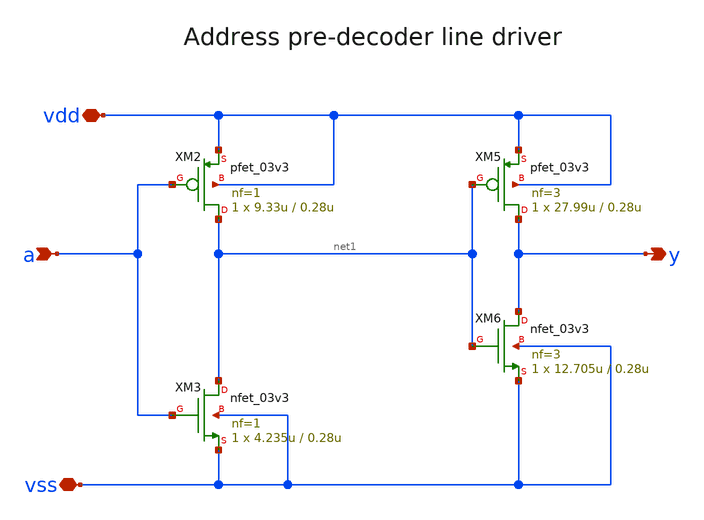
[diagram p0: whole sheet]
** sch_path: cells/gf180mcu_ocd_ip_sram__sram512x8m8wm1/xschem/ypredec1_ys_3v512x8m81.sch
**.subckt ypredec1_ys_3v512x8m81 vdd vss a y
*.iopin vdd
*.iopin vss
*.ipin a
*.opin y
XM2 net1 a vdd vdd pfet_03v3 L=0.28u W=9.33u nf=1 ad='int((nf+1)/2) * W/nf * 0.18u' as='int((nf+2)/2) * W/nf * 0.18u'
+ pd='2*int((nf+1)/2) * (W/nf + 0.18u)' ps='2*int((nf+2)/2) * (W/nf + 0.18u)' nrd='0.18u / W' nrs='0.18u / W'
+ sa=0 sb=0 sd=0 m=1
XM3 net1 a vss vss nfet_03v3 L=0.28u W=4.235u nf=1 ad='int((nf+1)/2) * W/nf * 0.18u' as='int((nf+2)/2) * W/nf * 0.18u'
+ pd='2*int((nf+1)/2) * (W/nf + 0.18u)' ps='2*int((nf+2)/2) * (W/nf + 0.18u)' nrd='0.18u / W' nrs='0.18u / W'
+ sa=0 sb=0 sd=0 m=1
XM5 y net1 vdd vdd pfet_03v3 L=0.28u W=27.99u nf=3 ad='int((nf+1)/2) * W/nf * 0.18u' as='int((nf+2)/2) * W/nf * 0.18u'
+ pd='2*int((nf+1)/2) * (W/nf + 0.18u)' ps='2*int((nf+2)/2) * (W/nf + 0.18u)' nrd='0.18u / W' nrs='0.18u / W'
+ sa=0 sb=0 sd=0 m=1
XM6 y net1 vss vss nfet_03v3 L=0.28u W=12.705u nf=3 ad='int((nf+1)/2) * W/nf * 0.18u' as='int((nf+2)/2) * W/nf * 0.18u'
+ pd='2*int((nf+1)/2) * (W/nf + 0.18u)' ps='2*int((nf+2)/2) * (W/nf + 0.18u)' nrd='0.18u / W' nrs='0.18u / W'
+ sa=0 sb=0 sd=0 m=1
**.ends
.end
